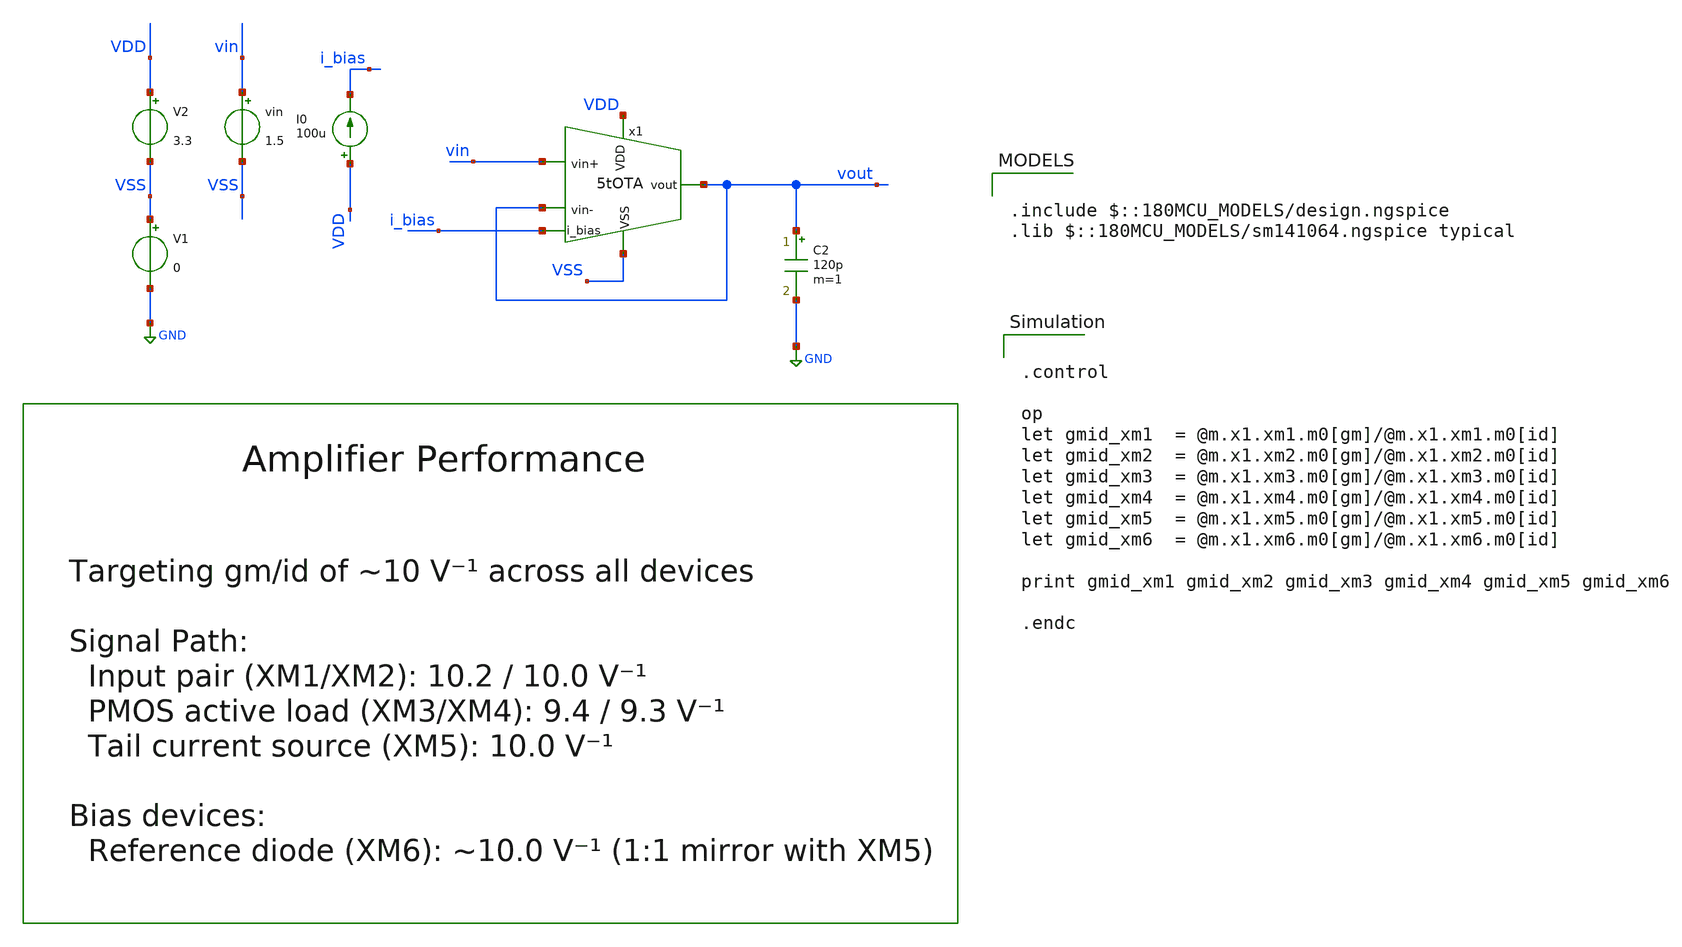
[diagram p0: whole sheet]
** sch_path: designs/libs/core_amps/ota_5t/tb/5tOTA_tb_gmid.sch
**.subckt 5tOTA_tb_gmid
V1 VSS GND 0
V2 VDD VSS 3.3
I0 VDD i_bias 100u
vin vin VSS 1.5
C2 vout GND 120p m=1
x1 VDD vout vin vout i_bias VSS 5tOTA
**** begin user architecture code

.include $::180MCU_MODELS/design.ngspice
.lib $::180MCU_MODELS/sm141064.ngspice typical



.control

op
let gmid_xm1  = @m.x1.xm1.m0[gm]/@m.x1.xm1.m0[id]
let gmid_xm2  = @m.x1.xm2.m0[gm]/@m.x1.xm2.m0[id]
let gmid_xm3  = @m.x1.xm3.m0[gm]/@m.x1.xm3.m0[id]
let gmid_xm4  = @m.x1.xm4.m0[gm]/@m.x1.xm4.m0[id]
let gmid_xm5  = @m.x1.xm5.m0[gm]/@m.x1.xm5.m0[id]
let gmid_xm6  = @m.x1.xm6.m0[gm]/@m.x1.xm6.m0[id]

print gmid_xm1 gmid_xm2 gmid_xm3 gmid_xm4 gmid_xm5 gmid_xm6

.endc


**** end user architecture code
**.ends

* expanding   symbol:  libs/core_amps/ota_5t/schem/5tOTA.sym # of pins=6
** sym_path: designs/5tOTA.sym
** sch_path: designs/5tOTA.sch
.subckt 5tOTA VDD vout vin+ vin- i_bias VSS
*.ipin VDD
*.opin vout
*.ipin i_bias
*.ipin vin+
*.ipin vin-
*.ipin VSS
XM1 net1 vin+ net2 VSS nfet_03v3 L=0.5u W=11.43u nf=1 ad='int((nf+1)/2) * W/nf * 0.18u' as='int((nf+2)/2) * W/nf * 0.18u'
+ pd='2*int((nf+1)/2) * (W/nf + 0.18u)' ps='2*int((nf+2)/2) * (W/nf + 0.18u)' nrd='0.18u / W' nrs='0.18u / W'
+ sa=0 sb=0 sd=0 m=1
XM2 vout vin- net2 VSS nfet_03v3 L=0.5u W=11.43u nf=1 ad='int((nf+1)/2) * W/nf * 0.18u' as='int((nf+2)/2) * W/nf * 0.18u'
+ pd='2*int((nf+1)/2) * (W/nf + 0.18u)' ps='2*int((nf+2)/2) * (W/nf + 0.18u)' nrd='0.18u / W' nrs='0.18u / W'
+ sa=0 sb=0 sd=0 m=1
XM3 net1 net1 VDD VDD pfet_03v3 L=0.5u W=22.86u nf=1 ad='int((nf+1)/2) * W/nf * 0.18u' as='int((nf+2)/2) * W/nf * 0.18u'
+ pd='2*int((nf+1)/2) * (W/nf + 0.18u)' ps='2*int((nf+2)/2) * (W/nf + 0.18u)' nrd='0.18u / W' nrs='0.18u / W'
+ sa=0 sb=0 sd=0 m=1
XM4 vout net1 VDD VDD pfet_03v3 L=0.5u W=22.86u nf=1 ad='int((nf+1)/2) * W/nf * 0.18u' as='int((nf+2)/2) * W/nf * 0.18u'
+ pd='2*int((nf+1)/2) * (W/nf + 0.18u)' ps='2*int((nf+2)/2) * (W/nf + 0.18u)' nrd='0.18u / W' nrs='0.18u / W'
+ sa=0 sb=0 sd=0 m=1
XM5 net2 i_bias VSS VSS nfet_03v3 L=0.5u W=22.86u nf=1 ad='int((nf+1)/2) * W/nf * 0.18u' as='int((nf+2)/2) * W/nf * 0.18u'
+ pd='2*int((nf+1)/2) * (W/nf + 0.18u)' ps='2*int((nf+2)/2) * (W/nf + 0.18u)' nrd='0.18u / W' nrs='0.18u / W'
+ sa=0 sb=0 sd=0 m=1
XM6 i_bias i_bias VSS VSS nfet_03v3 L=0.5u W=22.86u nf=1 ad='int((nf+1)/2) * W/nf * 0.18u' as='int((nf+2)/2) * W/nf * 0.18u'
+ pd='2*int((nf+1)/2) * (W/nf + 0.18u)' ps='2*int((nf+2)/2) * (W/nf + 0.18u)' nrd='0.18u / W' nrs='0.18u / W'
+ sa=0 sb=0 sd=0 m=1
.ends

.GLOBAL GND
.end
